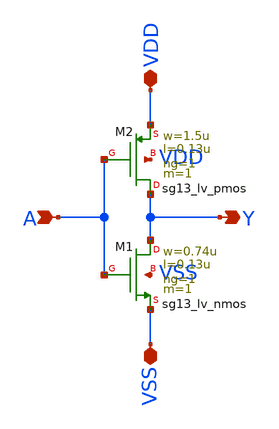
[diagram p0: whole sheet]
** sch_path: cdept-gui/tutorials/start/inv-sch/libs/work/inv/schematic/inv.sch
**.subckt inv A Y VDD VSS
*.ipin A
*.opin Y
*.iopin VDD
*.iopin VSS
XM2 Y A VDD VDD sg13_lv_pmos w=1.5u l=0.13u ng=1 m=1 mm_ok=1
XM1 Y A VSS VSS sg13_lv_nmos w=0.74u l=0.13u ng=1 m=1 mm_ok=1
**.ends
.end
